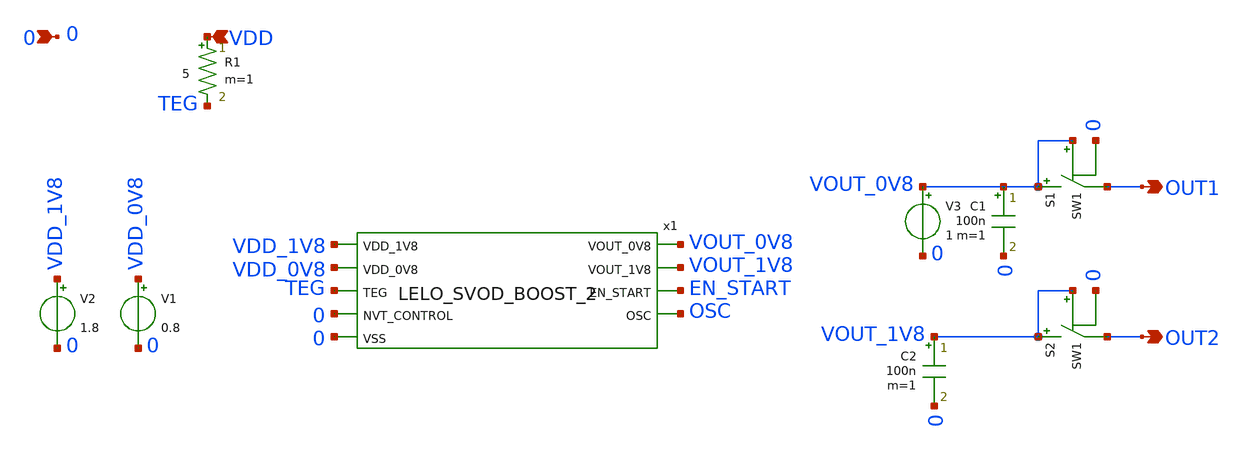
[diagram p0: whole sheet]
** sch_path: design/LELO_SVOD_SKY130A/LELO_SVOD_1V8_BOOST.sch
**.subckt LELO_SVOD_1V8_BOOST VDD 0 OUT2 OUT1
*.ipin VDD
*.ipin 0
*.opin OUT2
*.opin OUT1
R1 VDD TEG 5 m=1
V1 VDD_0V8 0 0.8
V2 VDD_1V8 0 1.8
S1 VOUT_0V8 OUT1 VOUT_0V8 0 SW1
S2 VOUT_1V8 OUT2 VOUT_1V8 0 SW1
x1 VOUT_0V8 VDD_1V8 VDD_0V8 TEG 0 0 VOUT_1V8 EN_START OSC LELO_SVOD_BOOST_2
V3 VOUT_0V8 0 1
C2 VOUT_1V8 0 100n m=1
C1 VOUT_0V8 0 100n m=1
**.ends
**** begin user architecture code
.MODEL SW1 SW   VT=1.8 VH=0.001  RON=0.001 ROFF=10G
**** end user architecture code
.end
